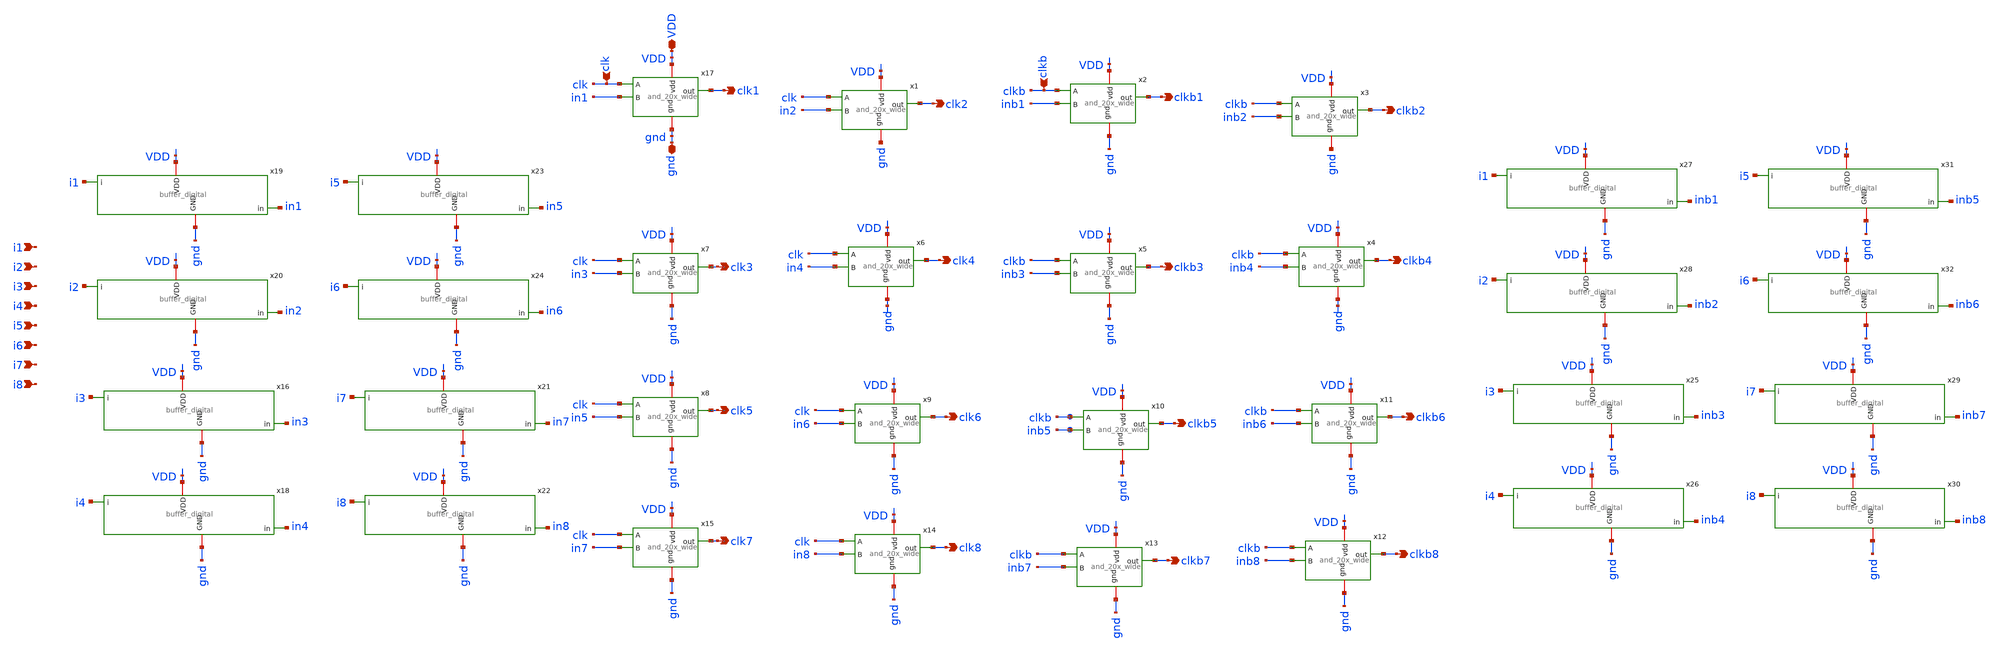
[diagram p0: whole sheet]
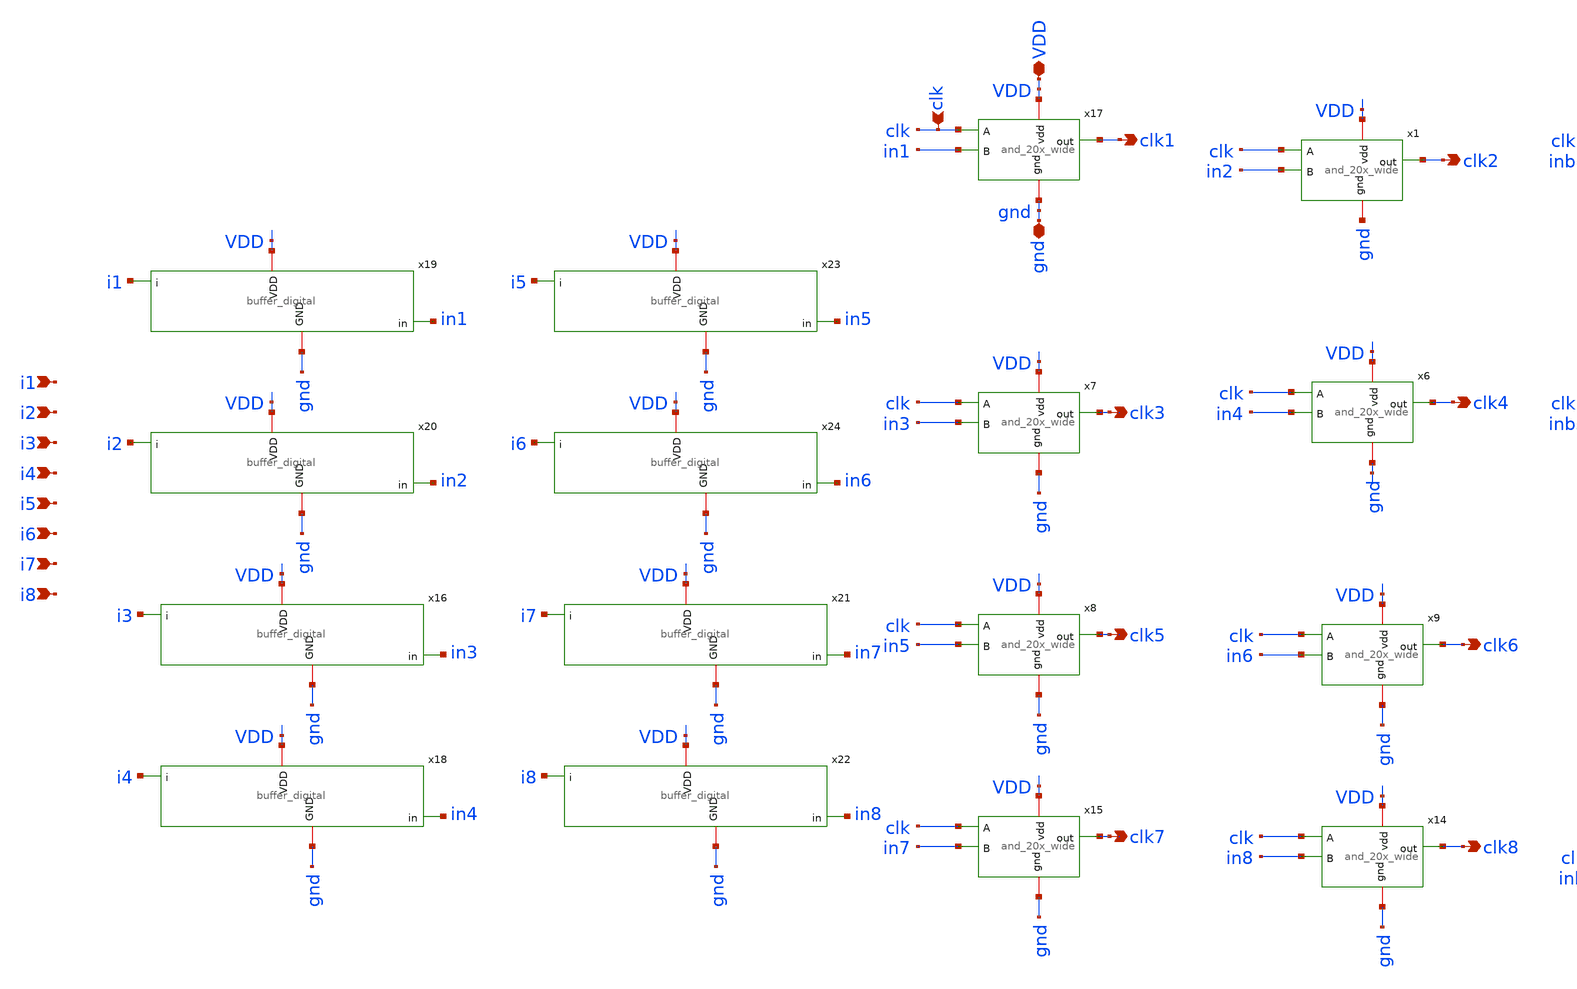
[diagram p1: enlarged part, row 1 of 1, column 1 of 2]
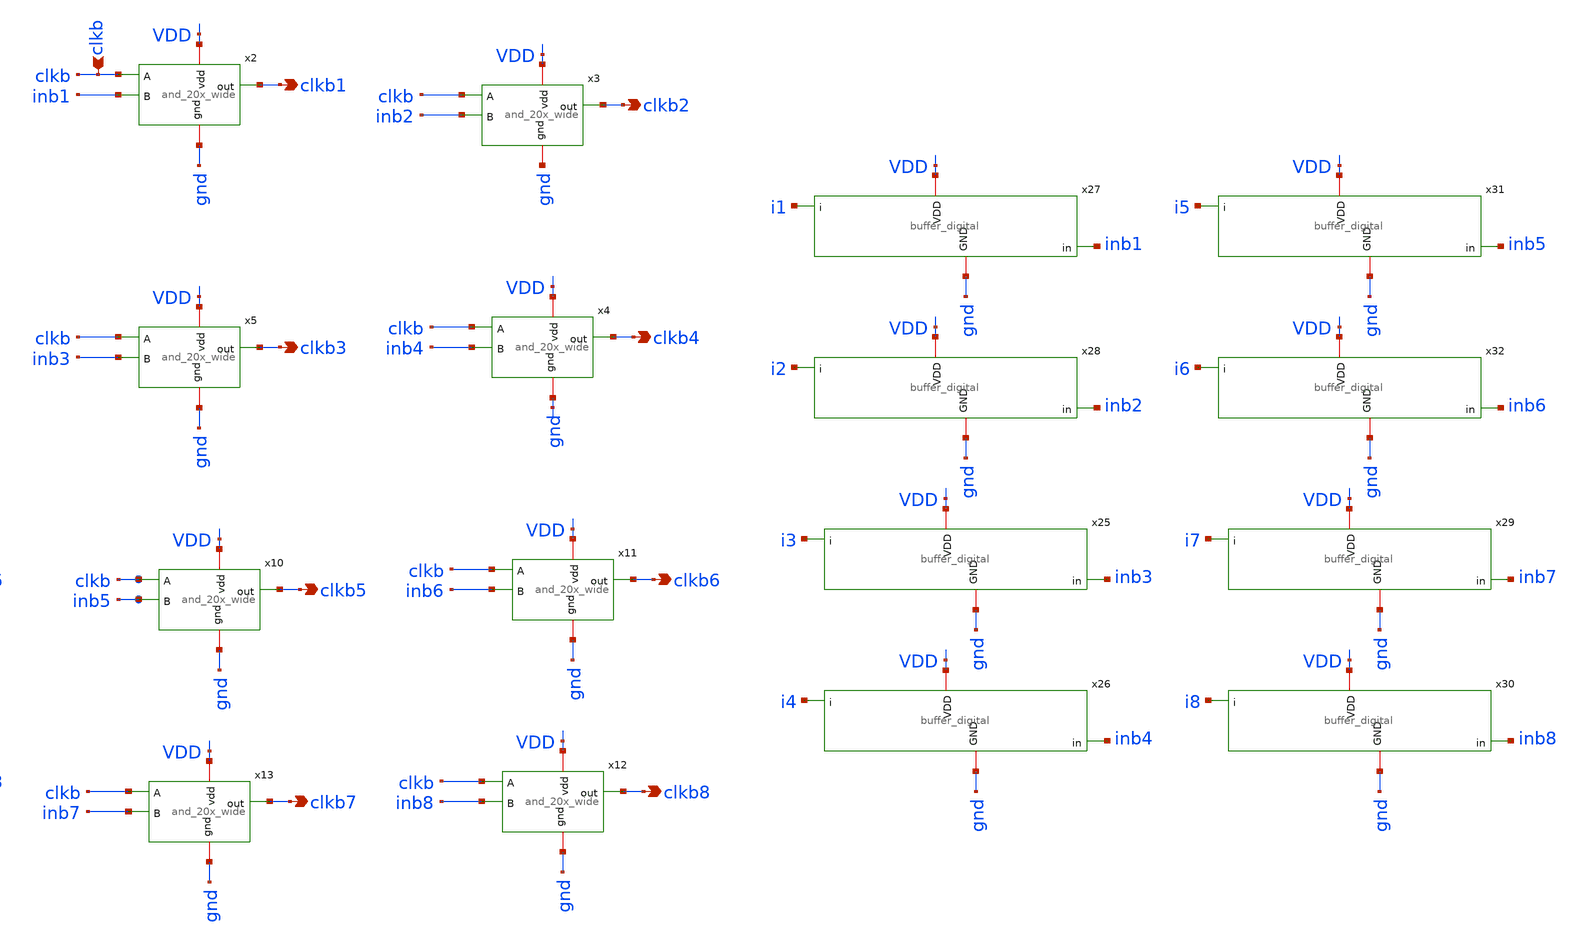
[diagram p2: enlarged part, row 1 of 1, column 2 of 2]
** sch_path: xschem/charge_pumps2/and_gates_8.sch
**.subckt and_gates_8 i1 clk VDD gnd clk1 clk2 clk3 clk4 clk5 clk6 clk7 clk8 clkb clkb1 clkb2 clkb3
*+ clkb4 clkb5 clkb6 clkb7 clkb8 i2 i3 i4 i5 i6 i7 i8
*.ipin i1
*.ipin clk
*.iopin VDD
*.iopin gnd
*.opin clk1
*.opin clk2
*.opin clk3
*.opin clk4
*.opin clk5
*.opin clk6
*.opin clk7
*.opin clk8
*.ipin clkb
*.opin clkb1
*.opin clkb2
*.opin clkb3
*.opin clkb4
*.opin clkb5
*.opin clkb6
*.opin clkb7
*.opin clkb8
*.ipin i2
*.ipin i3
*.ipin i4
*.ipin i5
*.ipin i6
*.ipin i7
*.ipin i8
x17 clk1 clk in1 VDD gnd and_20x_wide
x1 clk2 clk in2 VDD gnd and_20x_wide
x2 clkb1 clkb inb1 VDD gnd and_20x_wide
x3 clkb2 clkb inb2 VDD gnd and_20x_wide
x4 clkb4 clkb inb4 VDD gnd and_20x_wide
x5 clkb3 clkb inb3 VDD gnd and_20x_wide
x6 clk4 clk in4 VDD gnd and_20x_wide
x7 clk3 clk in3 VDD gnd and_20x_wide
x8 clk5 clk in5 VDD gnd and_20x_wide
x9 clk6 clk in6 VDD gnd and_20x_wide
x10 clkb5 clkb inb5 VDD gnd and_20x_wide
x11 clkb6 clkb inb6 VDD gnd and_20x_wide
x12 clkb8 clkb inb8 VDD gnd and_20x_wide
x13 clkb7 clkb inb7 VDD gnd and_20x_wide
x14 clk8 clk in8 VDD gnd and_20x_wide
x15 clk7 clk in7 VDD gnd and_20x_wide
x16 gnd VDD i3 in3 buffer_digital
x18 gnd VDD i4 in4 buffer_digital
x19 gnd VDD i1 in1 buffer_digital
x20 gnd VDD i2 in2 buffer_digital
x21 gnd VDD i7 in7 buffer_digital
x22 gnd VDD i8 in8 buffer_digital
x23 gnd VDD i5 in5 buffer_digital
x24 gnd VDD i6 in6 buffer_digital
x25 gnd VDD i3 inb3 buffer_digital
x26 gnd VDD i4 inb4 buffer_digital
x27 gnd VDD i1 inb1 buffer_digital
x28 gnd VDD i2 inb2 buffer_digital
x29 gnd VDD i7 inb7 buffer_digital
x30 gnd VDD i8 inb8 buffer_digital
x31 gnd VDD i5 inb5 buffer_digital
x32 gnd VDD i6 inb6 buffer_digital
**.ends
.end
